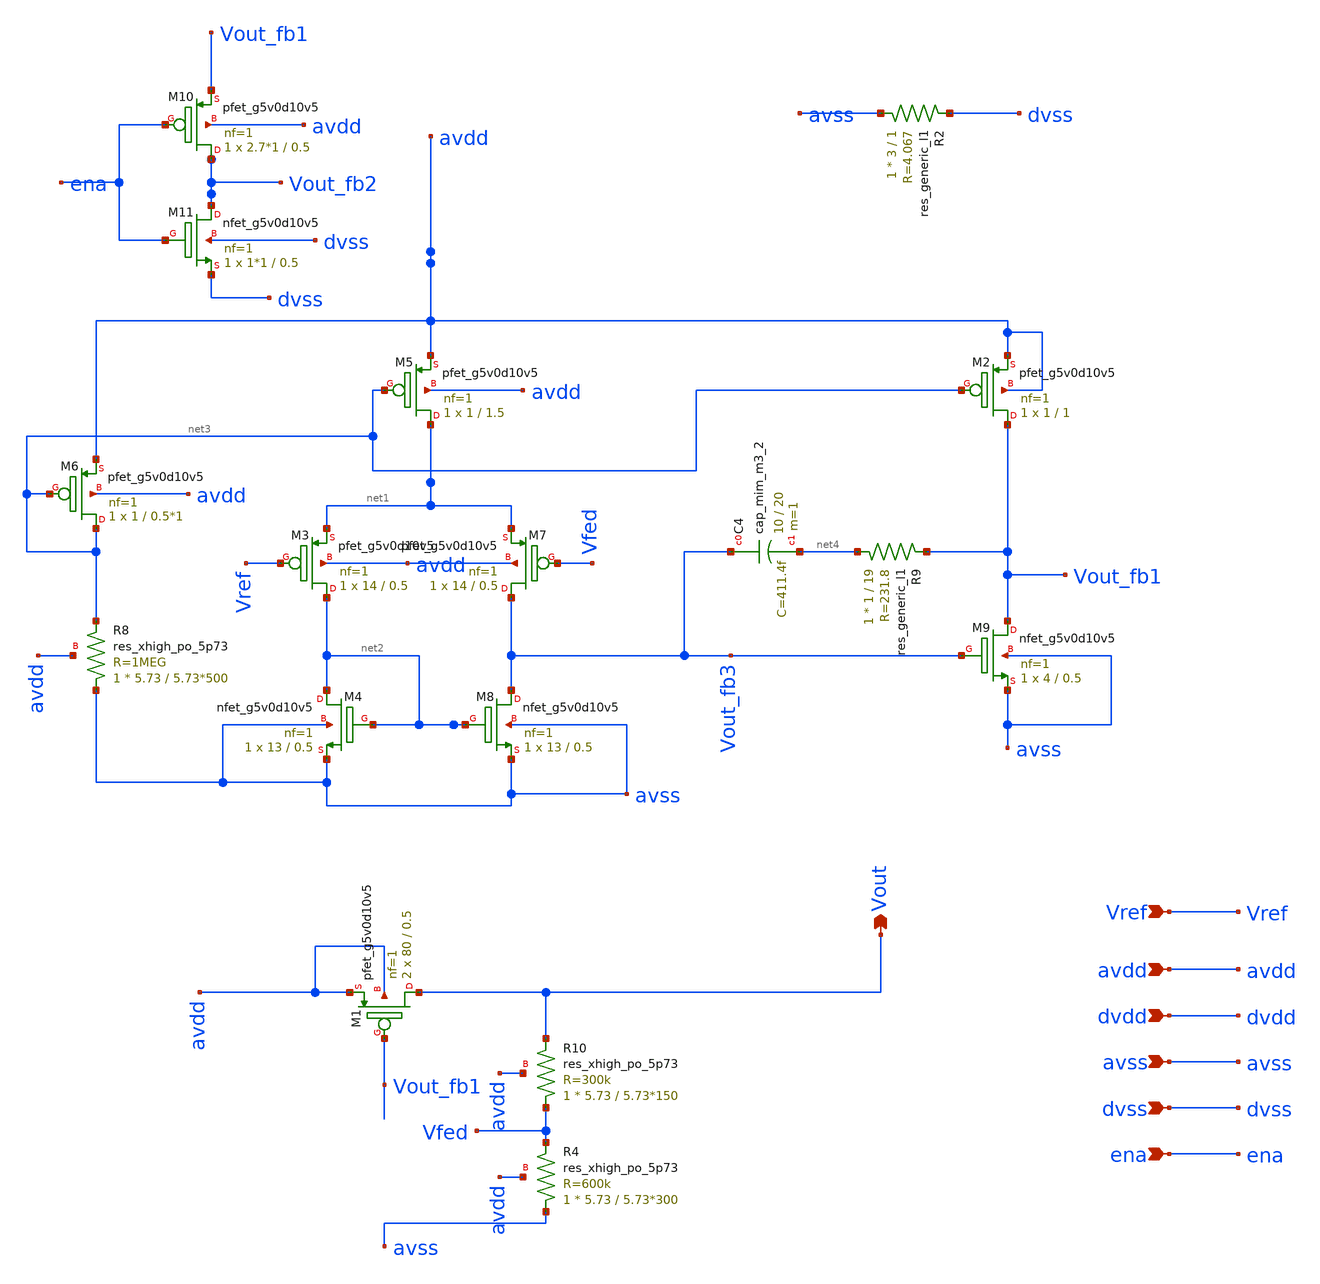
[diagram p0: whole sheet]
** sch_path: xschem/sky130_deser_ip_lowpowerLDO.sch
**.subckt sky130_deser_ip_lowpowerLDO avdd dvss dvdd avss ena Vref Vout
*.ipin avdd
*.ipin dvss
*.ipin dvdd
*.ipin avss
*.ipin ena
*.ipin Vref
*.opin Vout
XR10 Vfed Vout avdd sky130_fd_pr__res_xhigh_po_5p73 L=5.73*150 mult=1 m=1
XR4 avss Vfed avdd sky130_fd_pr__res_xhigh_po_5p73 L=5.73*300 mult=1 m=1
XR8 avss net3 avdd sky130_fd_pr__res_xhigh_po_5p73 L=5.73*500 mult=1 m=1
XC4 Vout_fb3 net4 sky130_fd_pr__cap_mim_m3_2 W=10 L=20 MF=1 m=1
R9 net4 Vout_fb1 sky130_fd_pr__res_generic_l1 W=1 L=19 m=1
XM6 net3 net3 avdd avdd sky130_fd_pr__pfet_g5v0d10v5 L=0.5*1 W=1 nf=1 ad='int((nf+1)/2) * W/nf * 0.29'
+ as='int((nf+2)/2) * W/nf * 0.29' pd='2*int((nf+1)/2) * (W/nf + 0.29)' ps='2*int((nf+2)/2) * (W/nf + 0.29)'
+ nrd='0.29 / W' nrs='0.29 / W' sa=0 sb=0 sd=0 mult=1 m=1
XM5 net1 net3 avdd avdd sky130_fd_pr__pfet_g5v0d10v5 L=1.5 W=1 nf=1 ad='int((nf+1)/2) * W/nf * 0.29'
+ as='int((nf+2)/2) * W/nf * 0.29' pd='2*int((nf+1)/2) * (W/nf + 0.29)' ps='2*int((nf+2)/2) * (W/nf + 0.29)'
+ nrd='0.29 / W' nrs='0.29 / W' sa=0 sb=0 sd=0 mult=1 m=1
XM2 Vout_fb1 net3 avdd avdd sky130_fd_pr__pfet_g5v0d10v5 L=1 W=1 nf=1 ad='int((nf+1)/2) * W/nf * 0.29'
+ as='int((nf+2)/2) * W/nf * 0.29' pd='2*int((nf+1)/2) * (W/nf + 0.29)' ps='2*int((nf+2)/2) * (W/nf + 0.29)'
+ nrd='0.29 / W' nrs='0.29 / W' sa=0 sb=0 sd=0 mult=1 m=1
XM7 Vout_fb3 Vfed net1 avdd sky130_fd_pr__pfet_g5v0d10v5 L=0.5 W=14 nf=1 ad='int((nf+1)/2) * W/nf * 0.29'
+ as='int((nf+2)/2) * W/nf * 0.29' pd='2*int((nf+1)/2) * (W/nf + 0.29)' ps='2*int((nf+2)/2) * (W/nf + 0.29)'
+ nrd='0.29 / W' nrs='0.29 / W' sa=0 sb=0 sd=0 mult=1 m=1
XM3 net2 Vref net1 avdd sky130_fd_pr__pfet_g5v0d10v5 L=0.5 W=14 nf=1 ad='int((nf+1)/2) * W/nf * 0.29'
+ as='int((nf+2)/2) * W/nf * 0.29' pd='2*int((nf+1)/2) * (W/nf + 0.29)' ps='2*int((nf+2)/2) * (W/nf + 0.29)'
+ nrd='0.29 / W' nrs='0.29 / W' sa=0 sb=0 sd=0 mult=1 m=1
XM1 Vout Vout_fb1 avdd avdd sky130_fd_pr__pfet_g5v0d10v5 L=0.5 W=80 nf=1 ad='int((nf+1)/2) * W/nf * 0.29'
+ as='int((nf+2)/2) * W/nf * 0.29' pd='2*int((nf+1)/2) * (W/nf + 0.29)' ps='2*int((nf+2)/2) * (W/nf + 0.29)'
+ nrd='0.29 / W' nrs='0.29 / W' sa=0 sb=0 sd=0 mult=2 m=2
XM8 Vout_fb3 net2 avss avss sky130_fd_pr__nfet_g5v0d10v5 L=0.5 W=13 nf=1 ad='int((nf+1)/2) * W/nf * 0.29'
+ as='int((nf+2)/2) * W/nf * 0.29' pd='2*int((nf+1)/2) * (W/nf + 0.29)' ps='2*int((nf+2)/2) * (W/nf + 0.29)'
+ nrd='0.29 / W' nrs='0.29 / W' sa=0 sb=0 sd=0 mult=1 m=1
XM9 Vout_fb1 Vout_fb3 avss avss sky130_fd_pr__nfet_g5v0d10v5 L=0.5 W=4 nf=1 ad='int((nf+1)/2) * W/nf * 0.29'
+ as='int((nf+2)/2) * W/nf * 0.29' pd='2*int((nf+1)/2) * (W/nf + 0.29)' ps='2*int((nf+2)/2) * (W/nf + 0.29)'
+ nrd='0.29 / W' nrs='0.29 / W' sa=0 sb=0 sd=0 mult=1 m=1
XM4 net2 net2 avss avss sky130_fd_pr__nfet_g5v0d10v5 L=0.5 W=13 nf=1 ad='int((nf+1)/2) * W/nf * 0.29'
+ as='int((nf+2)/2) * W/nf * 0.29' pd='2*int((nf+1)/2) * (W/nf + 0.29)' ps='2*int((nf+2)/2) * (W/nf + 0.29)'
+ nrd='0.29 / W' nrs='0.29 / W' sa=0 sb=0 sd=0 mult=1 m=1
XM10 Vout_fb2 ena Vout_fb1 avdd sky130_fd_pr__pfet_g5v0d10v5 L=0.5 W=2.7*1 nf=1 ad='int((nf+1)/2) * W/nf * 0.29'
+ as='int((nf+2)/2) * W/nf * 0.29' pd='2*int((nf+1)/2) * (W/nf + 0.29)' ps='2*int((nf+2)/2) * (W/nf + 0.29)'
+ nrd='0.29 / W' nrs='0.29 / W' sa=0 sb=0 sd=0 mult=1 m=1
XM11 Vout_fb2 ena dvss dvss sky130_fd_pr__nfet_g5v0d10v5 L=0.5 W=1*1 nf=1 ad='int((nf+1)/2) * W/nf * 0.29'
+ as='int((nf+2)/2) * W/nf * 0.29' pd='2*int((nf+1)/2) * (W/nf + 0.29)' ps='2*int((nf+2)/2) * (W/nf + 0.29)'
+ nrd='0.29 / W' nrs='0.29 / W' sa=0 sb=0 sd=0 mult=1 m=1
R2 avss dvss sky130_fd_pr__res_generic_l1 W=3 L=1 m=1
**.ends
.end
